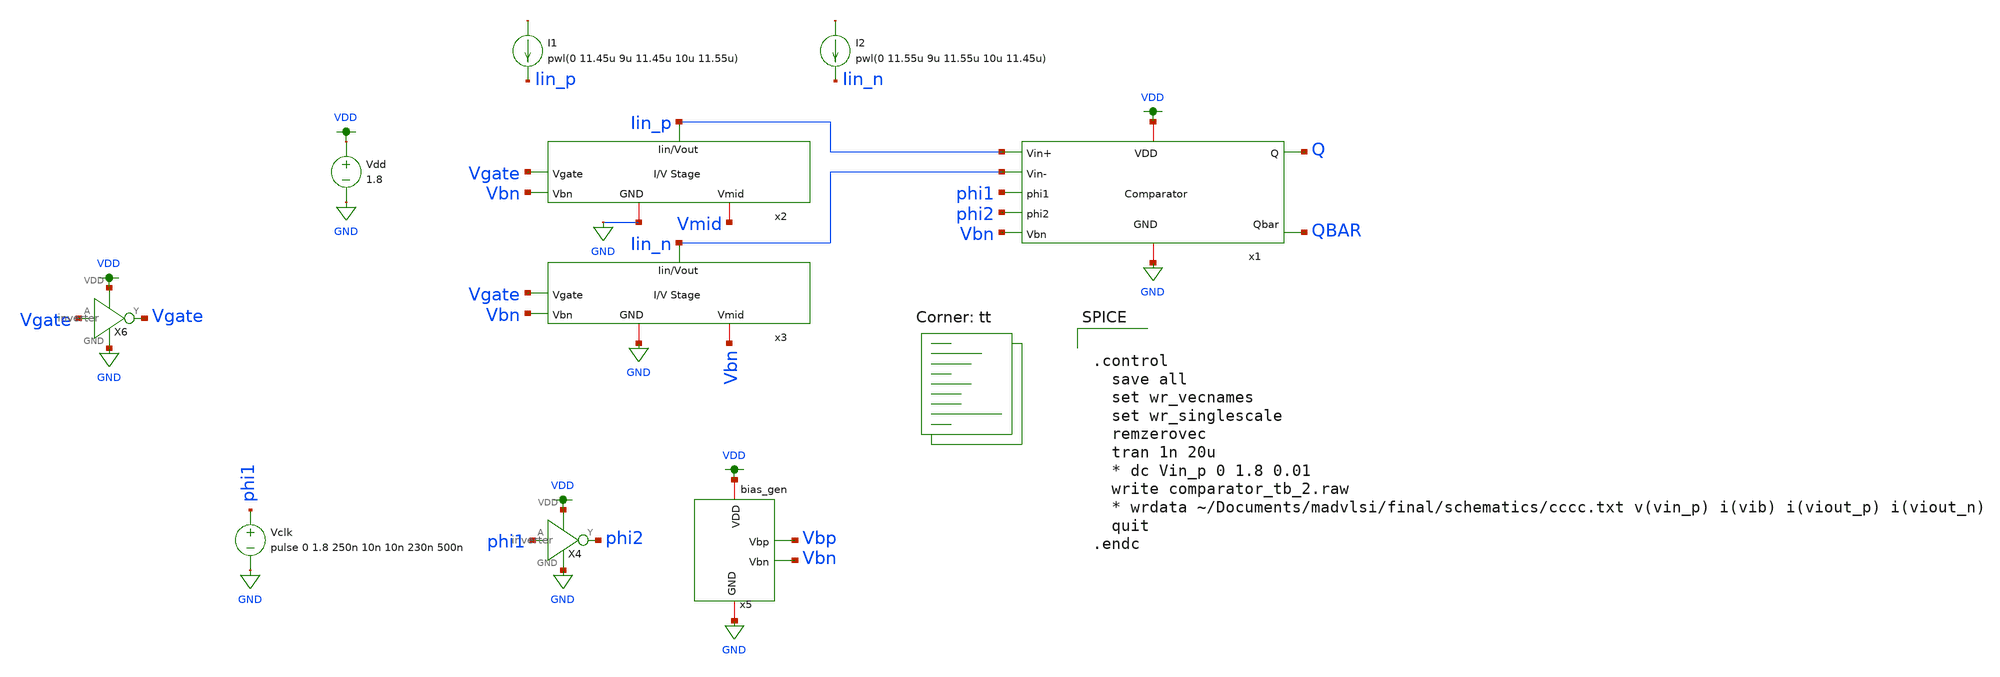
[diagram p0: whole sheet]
** sch_path: final/schematics/comparator_tb_2.sch
**.subckt comparator_tb_2
x1 VDD Vbn Iin_p Iin_n phi1 phi2 Q QBAR GND comparator
x2 Iin_p Vgate Vmid Vbn GND IV_converter
x3 Iin_n Vgate Vbn Vbn GND IV_converter
Vdd VDD GND 1.8
X4 VDD phi1 phi2 GND inverter
Vclk phi1 GND pulse 0 1.8 250n 10n 10n 230n 500n
x5 VDD Vbp Vbn GND bias_gen
I1 net1 Iin_p pwl(0 11.45u 9u 11.45u 10u 11.55u)
I2 net2 Iin_n pwl(0 11.55u 9u 11.55u 10u 11.45u)
X6 VDD Vgate Vgate GND inverter
**** begin user architecture code
.lib $::SKYWATER_MODELS/sky130.lib.spice tt


.control
  save all
  set wr_vecnames
  set wr_singlescale
  remzerovec
  tran 1n 20u
  * dc Vin_p 0 1.8 0.01
  write comparator_tb_2.raw
  * wrdata ~/Documents/madvlsi/final/schematics/cccc.txt v(vin_p) i(vib) i(viout_p) i(viout_n)
  quit
.endc


**** end user architecture code
**.ends

* expanding   symbol:  comparator.sym # of pins=9
** sym_path: final/schematics/comparator.sym
** sch_path: final/schematics/comparator.sch
.subckt comparator VDD Vbn Vin_p Vin_n phi1 phi2 Q Qbar GND
*.ipin Vin_p
*.ipin Vin_n
*.ipin Vbn
*.ipin phi1
*.ipin phi2
*.opin Q
*.opin Qbar
*.iopin VDD
*.iopin GND
XM2 net1 Vin_p net3 GND sky130_fd_pr__nfet_01v8 L={len} W={wid} nf=1 ad='int((nf+1)/2) * W/nf * 0.29'
+ as='int((nf+2)/2) * W/nf * 0.29' pd='2*int((nf+1)/2) * (W/nf + 0.29)' ps='2*int((nf+2)/2) * (W/nf + 0.29)'
+ nrd='0.29 / W' nrs='0.29 / W' sa=0 sb=0 sd=0 mult=1 m=1
XM3 VDD net3 net2 VDD sky130_fd_pr__pfet_01v8 L={len} W={wid} nf=1 ad='int((nf+1)/2) * W/nf * 0.29' as='int((nf+2)/2) * W/nf * 0.29'
+ pd='2*int((nf+1)/2) * (W/nf + 0.29)' ps='2*int((nf+2)/2) * (W/nf + 0.29)' nrd='0.29 / W' nrs='0.29 / W'
+ sa=0 sb=0 sd=0 mult=1 m=1
XM4 VDD net2 net3 VDD sky130_fd_pr__pfet_01v8 L={len} W={wid} nf=1 ad='int((nf+1)/2) * W/nf * 0.29' as='int((nf+2)/2) * W/nf * 0.29'
+ pd='2*int((nf+1)/2) * (W/nf + 0.29)' ps='2*int((nf+2)/2) * (W/nf + 0.29)' nrd='0.29 / W' nrs='0.29 / W'
+ sa=0 sb=0 sd=0 mult=1 m=1
XM7 net3 phi1 net2 VDD sky130_fd_pr__pfet_01v8 L={len} W={wid} nf=1 ad='int((nf+1)/2) * W/nf * 0.29'
+ as='int((nf+2)/2) * W/nf * 0.29' pd='2*int((nf+1)/2) * (W/nf + 0.29)' ps='2*int((nf+2)/2) * (W/nf + 0.29)'
+ nrd='0.29 / W' nrs='0.29 / W' sa=0 sb=0 sd=0 mult=1 m=1
XM5 net2 phi2 Q VDD sky130_fd_pr__pfet_01v8 L={len} W={wid} nf=1 ad='int((nf+1)/2) * W/nf * 0.29' as='int((nf+2)/2) * W/nf * 0.29'
+ pd='2*int((nf+1)/2) * (W/nf + 0.29)' ps='2*int((nf+2)/2) * (W/nf + 0.29)' nrd='0.29 / W' nrs='0.29 / W'
+ sa=0 sb=0 sd=0 mult=1 m=1
XM6 net3 phi2 Qbar VDD sky130_fd_pr__pfet_01v8 L={len} W={wid} nf=1 ad='int((nf+1)/2) * W/nf * 0.29'
+ as='int((nf+2)/2) * W/nf * 0.29' pd='2*int((nf+1)/2) * (W/nf + 0.29)' ps='2*int((nf+2)/2) * (W/nf + 0.29)'
+ nrd='0.29 / W' nrs='0.29 / W' sa=0 sb=0 sd=0 mult=1 m=1
XM1 net1 Vin_n net2 GND sky130_fd_pr__nfet_01v8 L={len} W={wid} nf=1 ad='int((nf+1)/2) * W/nf * 0.29'
+ as='int((nf+2)/2) * W/nf * 0.29' pd='2*int((nf+1)/2) * (W/nf + 0.29)' ps='2*int((nf+2)/2) * (W/nf + 0.29)'
+ nrd='0.29 / W' nrs='0.29 / W' sa=0 sb=0 sd=0 mult=1 m=1
XM8 GND Vbn net1 GND sky130_fd_pr__nfet_01v8 L={len} W={wid} nf=1 ad='int((nf+1)/2) * W/nf * 0.29' as='int((nf+2)/2) * W/nf * 0.29'
+ pd='2*int((nf+1)/2) * (W/nf + 0.29)' ps='2*int((nf+2)/2) * (W/nf + 0.29)' nrd='0.29 / W' nrs='0.29 / W'
+ sa=0 sb=0 sd=0 mult=1 m=1
XM9 GND phi2 Q GND sky130_fd_pr__nfet_01v8 L={len} W={wid} nf=1 ad='int((nf+1)/2) * W/nf * 0.29' as='int((nf+2)/2) * W/nf * 0.29'
+ pd='2*int((nf+1)/2) * (W/nf + 0.29)' ps='2*int((nf+2)/2) * (W/nf + 0.29)' nrd='0.29 / W' nrs='0.29 / W'
+ sa=0 sb=0 sd=0 mult=1 m=1
XM10 GND Q Qbar GND sky130_fd_pr__nfet_01v8 L={len} W={wid} nf=1 ad='int((nf+1)/2) * W/nf * 0.29' as='int((nf+2)/2) * W/nf * 0.29'
+ pd='2*int((nf+1)/2) * (W/nf + 0.29)' ps='2*int((nf+2)/2) * (W/nf + 0.29)' nrd='0.29 / W' nrs='0.29 / W'
+ sa=0 sb=0 sd=0 mult=1 m=1
XM11 GND Qbar Q GND sky130_fd_pr__nfet_01v8 L={len} W={wid} nf=1 ad='int((nf+1)/2) * W/nf * 0.29' as='int((nf+2)/2) * W/nf * 0.29'
+ pd='2*int((nf+1)/2) * (W/nf + 0.29)' ps='2*int((nf+2)/2) * (W/nf + 0.29)' nrd='0.29 / W' nrs='0.29 / W'
+ sa=0 sb=0 sd=0 mult=1 m=1
XM12 GND phi2 Qbar GND sky130_fd_pr__nfet_01v8 L={len} W={wid} nf=1 ad='int((nf+1)/2) * W/nf * 0.29'
+ as='int((nf+2)/2) * W/nf * 0.29' pd='2*int((nf+1)/2) * (W/nf + 0.29)' ps='2*int((nf+2)/2) * (W/nf + 0.29)'
+ nrd='0.29 / W' nrs='0.29 / W' sa=0 sb=0 sd=0 mult=1 m=1
**** begin user architecture code


.param wid=3 len=0.5


**** end user architecture code
.ends


* expanding   symbol:  IV_converter.sym # of pins=5
** sym_path: final/schematics/IV_converter.sym
** sch_path: final/schematics/IV_converter.sch
.subckt IV_converter Iin_Vout Vgate Vmid Vbn GND
*.iopin Iin_Vout
*.iopin GND
*.iopin Vmid
*.ipin Vbn
*.ipin Vgate
XM1 GND net1 Iin_Vout VDD sky130_fd_pr__pfet_01v8 L={len} W={wid} nf=1 ad='int((nf+1)/2) * W/nf * 0.29'
+ as='int((nf+2)/2) * W/nf * 0.29' pd='2*int((nf+1)/2) * (W/nf + 0.29)' ps='2*int((nf+2)/2) * (W/nf + 0.29)'
+ nrd='0.29 / W' nrs='0.29 / W' sa=0 sb=0 sd=0 mult=1 m=1
XM2 net1 net1 Vmid Vmid sky130_fd_pr__pfet_01v8 L={len} W={wid} nf=1 ad='int((nf+1)/2) * W/nf * 0.29'
+ as='int((nf+2)/2) * W/nf * 0.29' pd='2*int((nf+1)/2) * (W/nf + 0.29)' ps='2*int((nf+2)/2) * (W/nf + 0.29)'
+ nrd='0.29 / W' nrs='0.29 / W' sa=0 sb=0 sd=0 mult=1 m=1
XM3 net1 Vbn GND GND sky130_fd_pr__nfet_01v8 L={len} W={wid} nf=1 ad='int((nf+1)/2) * W/nf * 0.29' as='int((nf+2)/2) * W/nf * 0.29'
+ pd='2*int((nf+1)/2) * (W/nf + 0.29)' ps='2*int((nf+2)/2) * (W/nf + 0.29)' nrd='0.29 / W' nrs='0.29 / W'
+ sa=0 sb=0 sd=0 mult=1 m=1
XM4 Iin_Vout Vgate Vmid GND sky130_fd_pr__nfet_01v8 L=4 W=1 nf=1 ad='int((nf+1)/2) * W/nf * 0.29' as='int((nf+2)/2) * W/nf * 0.29'
+ pd='2*int((nf+1)/2) * (W/nf + 0.29)' ps='2*int((nf+2)/2) * (W/nf + 0.29)' nrd='0.29 / W' nrs='0.29 / W'
+ sa=0 sb=0 sd=0 mult=1 m=1
**** begin user architecture code


.param wid=3 len=0.5


**** end user architecture code
.ends


* expanding   symbol:  inverter.sym # of pins=4
** sym_path: final/schematics/inverter.sym
** sch_path: final/schematics/inverter.sch
.subckt inverter VDD A Y GND
*.ipin A
*.iopin VDD
*.iopin GND
*.opin Y
XM1 Y A GND GND sky130_fd_pr__nfet_01v8 L={len} W={wid} nf=1 ad='int((nf+1)/2) * W/nf * 0.29' as='int((nf+2)/2) * W/nf * 0.29'
+ pd='2*int((nf+1)/2) * (W/nf + 0.29)' ps='2*int((nf+2)/2) * (W/nf + 0.29)' nrd='0.29 / W' nrs='0.29 / W'
+ sa=0 sb=0 sd=0 mult=1 m=1
XM2 Y A VDD VDD sky130_fd_pr__pfet_01v8 L={len} W={wid} nf=1 ad='int((nf+1)/2) * W/nf * 0.29' as='int((nf+2)/2) * W/nf * 0.29'
+ pd='2*int((nf+1)/2) * (W/nf + 0.29)' ps='2*int((nf+2)/2) * (W/nf + 0.29)' nrd='0.29 / W' nrs='0.29 / W'
+ sa=0 sb=0 sd=0 mult=1 m=1
**** begin user architecture code


.param wid=3 len=0.5


**** end user architecture code
.ends


* expanding   symbol:  /home/dt/Documents/madvlsi/final/schematics/bias_gen/bias_gen.sym # of pins=4
** sym_path: final/schematics/bias_gen/bias_gen.sym
** sch_path: final/schematics/bias_gen/bias_gen.sch
.subckt bias_gen VDD Vbp Vbn GND
*.iopin VDD
*.opin Vbp
*.iopin GND
*.opin Vbn
**** begin user architecture code

.param len=0.5 wid=3

**** end user architecture code
XM10 net3 net1 net1 GND sky130_fd_pr__nfet_01v8 L={len} W={wid} nf=1 ad='int((nf+1)/2) * W/nf * 0.29'
+ as='int((nf+2)/2) * W/nf * 0.29' pd='2*int((nf+1)/2) * (W/nf + 0.29)' ps='2*int((nf+2)/2) * (W/nf + 0.29)'
+ nrd='0.29 / W' nrs='0.29 / W' sa=0 sb=0 sd=0 mult=10 m=10
XM11 Vbn Vbn GND GND sky130_fd_pr__nfet_01v8 L={len} W={wid} nf=1 ad='int((nf+1)/2) * W/nf * 0.29' as='int((nf+2)/2) * W/nf * 0.29'
+ pd='2*int((nf+1)/2) * (W/nf + 0.29)' ps='2*int((nf+2)/2) * (W/nf + 0.29)' nrd='0.29 / W' nrs='0.29 / W'
+ sa=0 sb=0 sd=0 mult=1 m=1
XM12 GND Vbp GND GND sky130_fd_pr__nfet_01v8 L=10 W=10 nf=1 ad='int((nf+1)/2) * W/nf * 0.29' as='int((nf+2)/2) * W/nf * 0.29'
+ pd='2*int((nf+1)/2) * (W/nf + 0.29)' ps='2*int((nf+2)/2) * (W/nf + 0.29)' nrd='0.29 / W' nrs='0.29 / W'
+ sa=0 sb=0 sd=0 mult=1 m=1
XM13 VDD Vbp net1 VDD sky130_fd_pr__pfet_01v8 L={len} W={wid} nf=1 ad='int((nf+1)/2) * W/nf * 0.29' as='int((nf+2)/2) * W/nf * 0.29'
+ pd='2*int((nf+1)/2) * (W/nf + 0.29)' ps='2*int((nf+2)/2) * (W/nf + 0.29)' nrd='0.29 / W' nrs='0.29 / W'
+ sa=0 sb=0 sd=0 mult=1 m=1
XM14 GND Vbn Vbp GND sky130_fd_pr__nfet_01v8 L={len} W={wid} nf=1 ad='int((nf+1)/2) * W/nf * 0.29' as='int((nf+2)/2) * W/nf * 0.29'
+ pd='2*int((nf+1)/2) * (W/nf + 0.29)' ps='2*int((nf+2)/2) * (W/nf + 0.29)' nrd='0.29 / W' nrs='0.29 / W'
+ sa=0 sb=0 sd=0 mult=1 m=1
XM15 net2 net1 GND GND sky130_fd_pr__nfet_01v8 L={len} W={wid} nf=1 ad='int((nf+1)/2) * W/nf * 0.29'
+ as='int((nf+2)/2) * W/nf * 0.29' pd='2*int((nf+1)/2) * (W/nf + 0.29)' ps='2*int((nf+2)/2) * (W/nf + 0.29)'
+ nrd='0.29 / W' nrs='0.29 / W' sa=0 sb=0 sd=0 mult=1 m=1
XM16 VDD net2 net2 VDD sky130_fd_pr__pfet_01v8 L={len} W={wid} nf=1 ad='int((nf+1)/2) * W/nf * 0.29'
+ as='int((nf+2)/2) * W/nf * 0.29' pd='2*int((nf+1)/2) * (W/nf + 0.29)' ps='2*int((nf+2)/2) * (W/nf + 0.29)'
+ nrd='0.29 / W' nrs='0.29 / W' sa=0 sb=0 sd=0 mult=1 m=1
XM17 Vbp net2 VDD VDD sky130_fd_pr__pfet_01v8 L={len} W={wid} nf=1 ad='int((nf+1)/2) * W/nf * 0.29' as='int((nf+2)/2) * W/nf * 0.29'
+ pd='2*int((nf+1)/2) * (W/nf + 0.29)' ps='2*int((nf+2)/2) * (W/nf + 0.29)' nrd='0.29 / W' nrs='0.29 / W'
+ sa=0 sb=0 sd=0 mult=1 m=1
XM18 Vbn Vbp VDD VDD sky130_fd_pr__pfet_01v8 L={len} W={wid} nf=1 ad='int((nf+1)/2) * W/nf * 0.29' as='int((nf+2)/2) * W/nf * 0.29'
+ pd='2*int((nf+1)/2) * (W/nf + 0.29)' ps='2*int((nf+2)/2) * (W/nf + 0.29)' nrd='0.29 / W' nrs='0.29 / W'
+ sa=0 sb=0 sd=0 mult=1 m=1
XR2 GND net3 GND sky130_fd_pr__res_high_po_0p35 L=9 mult=1 m=1
.ends

.GLOBAL GND
.GLOBAL VDD
.end
